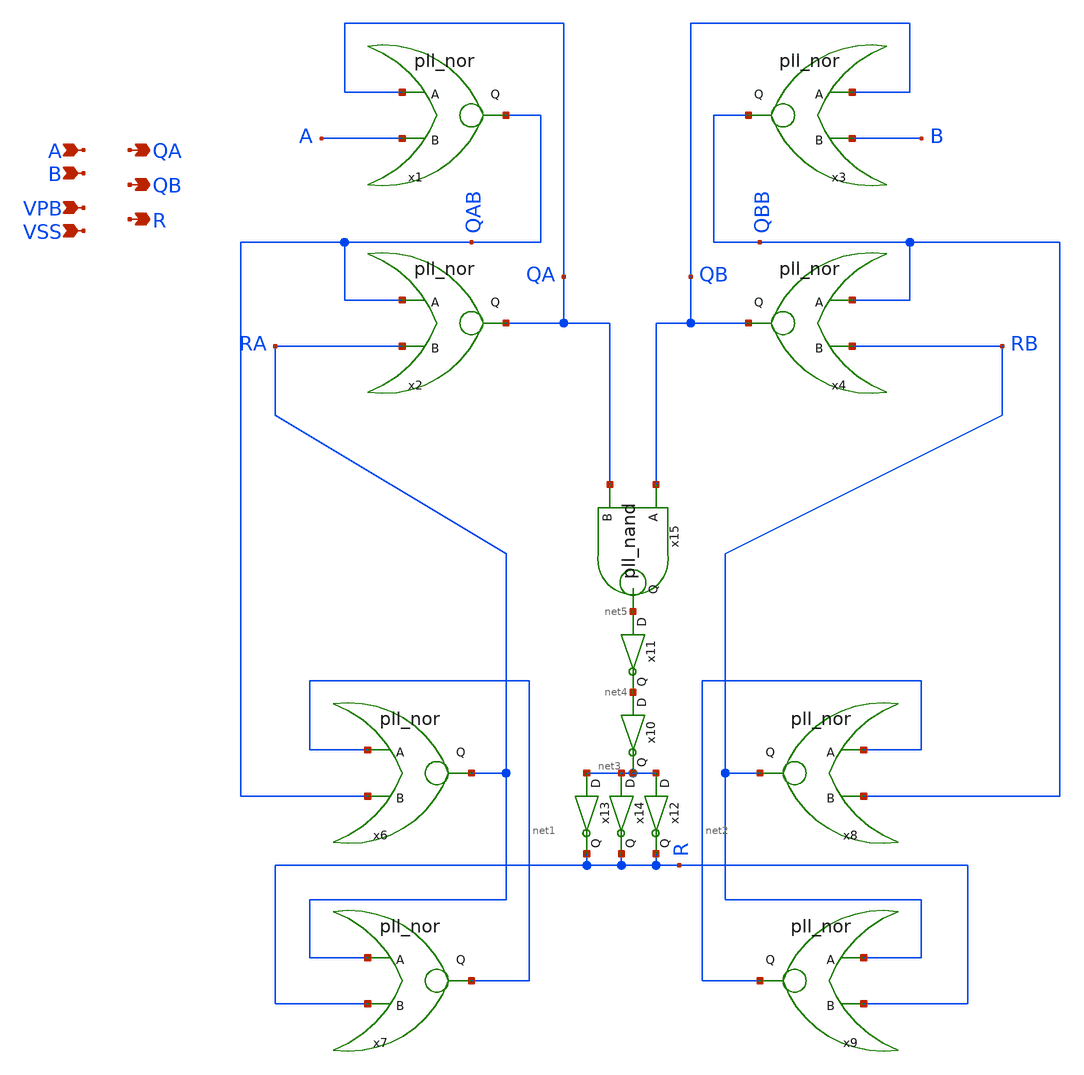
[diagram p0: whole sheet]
** sch_path: xschem/pll_pfd.sch
**.subckt pll_pfd A B VPB VSS QA QB R
*.ipin A
*.ipin B
*.ipin VPB
*.ipin VSS
*.opin QA
*.opin QB
*.opin R
x1 QA A QAB VSS VDD pll_nor
x2 QAB RA QA VSS VDD pll_nor
x3 QB B QBB VSS VDD pll_nor
x4 QBB RB QB VSS VDD pll_nor
x6 net1 QAB RA VSS VDD pll_nor
x7 RA R net1 VSS VDD pll_nor
x8 net2 QBB RB VSS VDD pll_nor
x9 RB R net2 VSS VDD pll_nor
x10 net4 net3 VDD VSS pll_inv1
x11 net5 net4 VDD VSS pll_inv1
x12 net3 R VDD VSS pll_inv1
x13 net3 R VDD VSS pll_inv1
x14 net3 R VDD VSS pll_inv1
x15 QB QA net5 VDD VSS pll_nand
**.ends
.end
